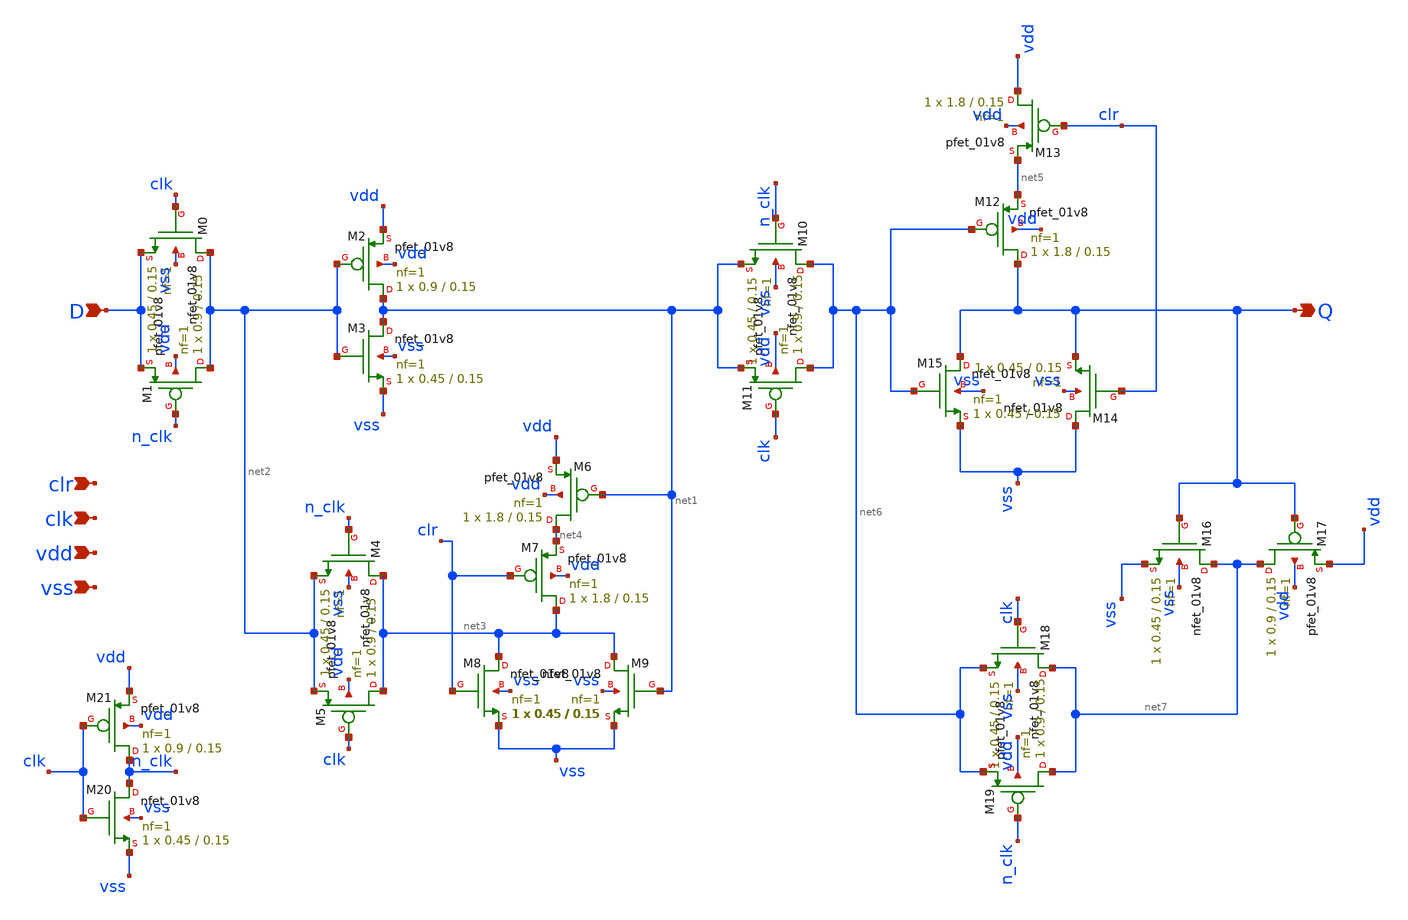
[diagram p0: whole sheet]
** sch_path: xschem/flipflop.sch
**.subckt flipflop clk D vdd vss clr Q
*.ipin clk
*.ipin D
*.ipin vdd
*.ipin vss
*.ipin clr
*.opin Q
XM3 net1 net2 vss vss sky130_fd_pr__nfet_01v8 L=0.15 W=0.45 nf=1 ad='int((nf+1)/2) * W/nf * 0.29' as='int((nf+2)/2) * W/nf * 0.29'
+ pd='2*int((nf+1)/2) * (W/nf + 0.29)' ps='2*int((nf+2)/2) * (W/nf + 0.29)' nrd='0.29 / W' nrs='0.29 / W'
+ sa=0 sb=0 sd=0 mult=1 m=1
XM2 net1 net2 vdd vdd sky130_fd_pr__pfet_01v8 L=0.15 W=0.9 nf=1 ad='int((nf+1)/2) * W/nf * 0.29' as='int((nf+2)/2) * W/nf * 0.29'
+ pd='2*int((nf+1)/2) * (W/nf + 0.29)' ps='2*int((nf+2)/2) * (W/nf + 0.29)' nrd='0.29 / W' nrs='0.29 / W'
+ sa=0 sb=0 sd=0 mult=1 m=1
XM1 net2 n_clk D vdd sky130_fd_pr__pfet_01v8 L=0.15 W=0.9 nf=1 ad='int((nf+1)/2) * W/nf * 0.29' as='int((nf+2)/2) * W/nf * 0.29'
+ pd='2*int((nf+1)/2) * (W/nf + 0.29)' ps='2*int((nf+2)/2) * (W/nf + 0.29)' nrd='0.29 / W' nrs='0.29 / W'
+ sa=0 sb=0 sd=0 mult=1 m=1
XM0 net2 clk D vss sky130_fd_pr__nfet_01v8 L=0.15 W=0.45 nf=1 ad='int((nf+1)/2) * W/nf * 0.29' as='int((nf+2)/2) * W/nf * 0.29'
+ pd='2*int((nf+1)/2) * (W/nf + 0.29)' ps='2*int((nf+2)/2) * (W/nf + 0.29)' nrd='0.29 / W' nrs='0.29 / W'
+ sa=0 sb=0 sd=0 mult=1 m=1
XM5 net3 clk net2 vdd sky130_fd_pr__pfet_01v8 L=0.15 W=0.9 nf=1 ad='int((nf+1)/2) * W/nf * 0.29' as='int((nf+2)/2) * W/nf * 0.29'
+ pd='2*int((nf+1)/2) * (W/nf + 0.29)' ps='2*int((nf+2)/2) * (W/nf + 0.29)' nrd='0.29 / W' nrs='0.29 / W'
+ sa=0 sb=0 sd=0 mult=1 m=1
XM4 net3 n_clk net2 vss sky130_fd_pr__nfet_01v8 L=0.15 W=0.45 nf=1 ad='int((nf+1)/2) * W/nf * 0.29' as='int((nf+2)/2) * W/nf * 0.29'
+ pd='2*int((nf+1)/2) * (W/nf + 0.29)' ps='2*int((nf+2)/2) * (W/nf + 0.29)' nrd='0.29 / W' nrs='0.29 / W'
+ sa=0 sb=0 sd=0 mult=1 m=1
XM6 net4 net1 vdd vdd sky130_fd_pr__pfet_01v8 L=0.15 W=1.8 nf=1 ad='int((nf+1)/2) * W/nf * 0.29' as='int((nf+2)/2) * W/nf * 0.29'
+ pd='2*int((nf+1)/2) * (W/nf + 0.29)' ps='2*int((nf+2)/2) * (W/nf + 0.29)' nrd='0.29 / W' nrs='0.29 / W'
+ sa=0 sb=0 sd=0 mult=1 m=1
XM7 net3 clr net4 vdd sky130_fd_pr__pfet_01v8 L=0.15 W=1.8 nf=1 ad='int((nf+1)/2) * W/nf * 0.29' as='int((nf+2)/2) * W/nf * 0.29'
+ pd='2*int((nf+1)/2) * (W/nf + 0.29)' ps='2*int((nf+2)/2) * (W/nf + 0.29)' nrd='0.29 / W' nrs='0.29 / W'
+ sa=0 sb=0 sd=0 mult=1 m=1
XM8 net3 clr vss vss sky130_fd_pr__nfet_01v8 L=0.15 W=0.45 nf=1 ad='int((nf+1)/2) * W/nf * 0.29' as='int((nf+2)/2) * W/nf * 0.29'
+ pd='2*int((nf+1)/2) * (W/nf + 0.29)' ps='2*int((nf+2)/2) * (W/nf + 0.29)' nrd='0.29 / W' nrs='0.29 / W'
+ sa=0 sb=0 sd=0 mult=1 m=1
XM9 net3 net1 vss vss sky130_fd_pr__nfet_01v8 L=0.15 W=0.45 nf=1 ad='int((nf+1)/2) * W/nf * 0.29' as='int((nf+2)/2) * W/nf * 0.29'
+ pd='2*int((nf+1)/2) * (W/nf + 0.29)' ps='2*int((nf+2)/2) * (W/nf + 0.29)' nrd='0.29 / W' nrs='0.29 / W'
+ sa=0 sb=0 sd=0 mult=1 m=1
XM10 net6 n_clk net1 vss sky130_fd_pr__nfet_01v8 L=0.15 W=0.45 nf=1 ad='int((nf+1)/2) * W/nf * 0.29'
+ as='int((nf+2)/2) * W/nf * 0.29' pd='2*int((nf+1)/2) * (W/nf + 0.29)' ps='2*int((nf+2)/2) * (W/nf + 0.29)'
+ nrd='0.29 / W' nrs='0.29 / W' sa=0 sb=0 sd=0 mult=1 m=1
XM11 net6 clk net1 vdd sky130_fd_pr__pfet_01v8 L=0.15 W=0.9 nf=1 ad='int((nf+1)/2) * W/nf * 0.29' as='int((nf+2)/2) * W/nf * 0.29'
+ pd='2*int((nf+1)/2) * (W/nf + 0.29)' ps='2*int((nf+2)/2) * (W/nf + 0.29)' nrd='0.29 / W' nrs='0.29 / W'
+ sa=0 sb=0 sd=0 mult=1 m=1
XM12 Q net6 net5 vdd sky130_fd_pr__pfet_01v8 L=0.15 W=1.8 nf=1 ad='int((nf+1)/2) * W/nf * 0.29' as='int((nf+2)/2) * W/nf * 0.29'
+ pd='2*int((nf+1)/2) * (W/nf + 0.29)' ps='2*int((nf+2)/2) * (W/nf + 0.29)' nrd='0.29 / W' nrs='0.29 / W'
+ sa=0 sb=0 sd=0 mult=1 m=1
XM13 vdd clr net5 vdd sky130_fd_pr__pfet_01v8 L=0.15 W=1.8 nf=1 ad='int((nf+1)/2) * W/nf * 0.29' as='int((nf+2)/2) * W/nf * 0.29'
+ pd='2*int((nf+1)/2) * (W/nf + 0.29)' ps='2*int((nf+2)/2) * (W/nf + 0.29)' nrd='0.29 / W' nrs='0.29 / W'
+ sa=0 sb=0 sd=0 mult=1 m=1
XM14 vss clr Q vss sky130_fd_pr__nfet_01v8 L=0.15 W=0.45 nf=1 ad='int((nf+1)/2) * W/nf * 0.29' as='int((nf+2)/2) * W/nf * 0.29'
+ pd='2*int((nf+1)/2) * (W/nf + 0.29)' ps='2*int((nf+2)/2) * (W/nf + 0.29)' nrd='0.29 / W' nrs='0.29 / W'
+ sa=0 sb=0 sd=0 mult=1 m=1
XM15 Q net6 vss vss sky130_fd_pr__nfet_01v8 L=0.15 W=0.45 nf=1 ad='int((nf+1)/2) * W/nf * 0.29' as='int((nf+2)/2) * W/nf * 0.29'
+ pd='2*int((nf+1)/2) * (W/nf + 0.29)' ps='2*int((nf+2)/2) * (W/nf + 0.29)' nrd='0.29 / W' nrs='0.29 / W'
+ sa=0 sb=0 sd=0 mult=1 m=1
XM16 net7 Q vss vss sky130_fd_pr__nfet_01v8 L=0.15 W=0.45 nf=1 ad='int((nf+1)/2) * W/nf * 0.29' as='int((nf+2)/2) * W/nf * 0.29'
+ pd='2*int((nf+1)/2) * (W/nf + 0.29)' ps='2*int((nf+2)/2) * (W/nf + 0.29)' nrd='0.29 / W' nrs='0.29 / W'
+ sa=0 sb=0 sd=0 mult=1 m=1
XM17 net7 Q vdd vdd sky130_fd_pr__pfet_01v8 L=0.15 W=0.9 nf=1 ad='int((nf+1)/2) * W/nf * 0.29' as='int((nf+2)/2) * W/nf * 0.29'
+ pd='2*int((nf+1)/2) * (W/nf + 0.29)' ps='2*int((nf+2)/2) * (W/nf + 0.29)' nrd='0.29 / W' nrs='0.29 / W'
+ sa=0 sb=0 sd=0 mult=1 m=1
XM18 net7 clk net6 vss sky130_fd_pr__nfet_01v8 L=0.15 W=0.45 nf=1 ad='int((nf+1)/2) * W/nf * 0.29' as='int((nf+2)/2) * W/nf * 0.29'
+ pd='2*int((nf+1)/2) * (W/nf + 0.29)' ps='2*int((nf+2)/2) * (W/nf + 0.29)' nrd='0.29 / W' nrs='0.29 / W'
+ sa=0 sb=0 sd=0 mult=1 m=1
XM19 net7 n_clk net6 vdd sky130_fd_pr__pfet_01v8 L=0.15 W=0.9 nf=1 ad='int((nf+1)/2) * W/nf * 0.29' as='int((nf+2)/2) * W/nf * 0.29'
+ pd='2*int((nf+1)/2) * (W/nf + 0.29)' ps='2*int((nf+2)/2) * (W/nf + 0.29)' nrd='0.29 / W' nrs='0.29 / W'
+ sa=0 sb=0 sd=0 mult=1 m=1
XM20 n_clk clk vss vss sky130_fd_pr__nfet_01v8 L=0.15 W=0.45 nf=1 ad='int((nf+1)/2) * W/nf * 0.29' as='int((nf+2)/2) * W/nf * 0.29'
+ pd='2*int((nf+1)/2) * (W/nf + 0.29)' ps='2*int((nf+2)/2) * (W/nf + 0.29)' nrd='0.29 / W' nrs='0.29 / W'
+ sa=0 sb=0 sd=0 mult=1 m=1
XM21 n_clk clk vdd vdd sky130_fd_pr__pfet_01v8 L=0.15 W=0.9 nf=1 ad='int((nf+1)/2) * W/nf * 0.29' as='int((nf+2)/2) * W/nf * 0.29'
+ pd='2*int((nf+1)/2) * (W/nf + 0.29)' ps='2*int((nf+2)/2) * (W/nf + 0.29)' nrd='0.29 / W' nrs='0.29 / W'
+ sa=0 sb=0 sd=0 mult=1 m=1
**.ends
.end
